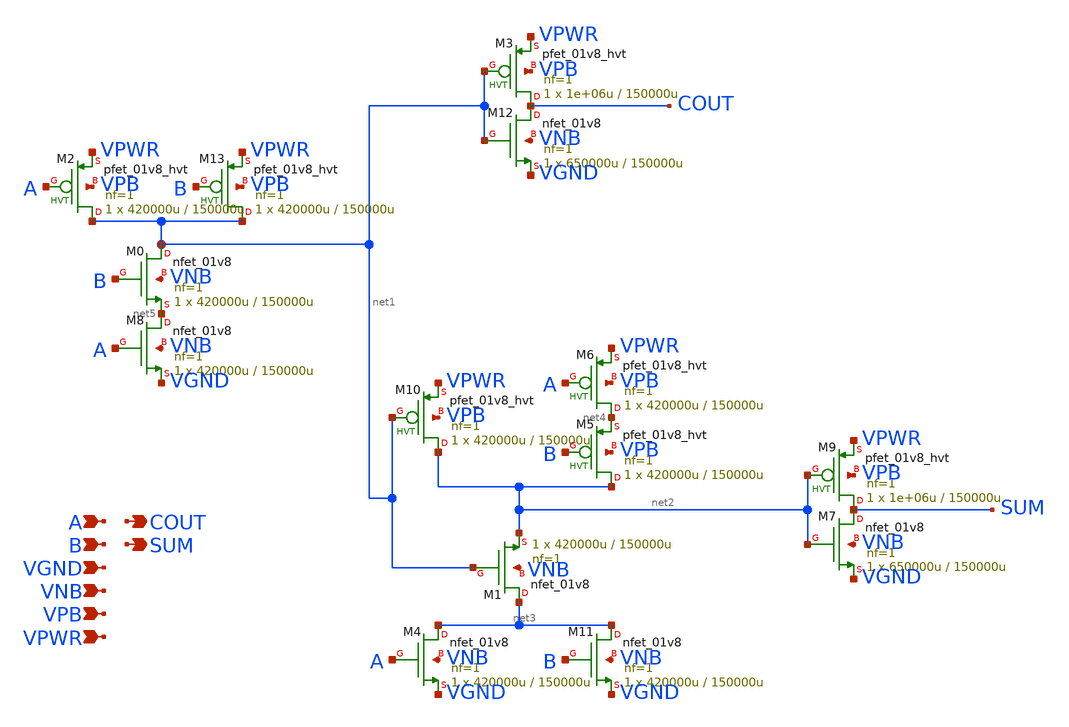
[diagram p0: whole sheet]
** sch_path: schematics/ha/sky130_fd_sc_hd__ha_1.sch
**.subckt sky130_fd_sc_hd__ha_1 A B VGND VNB VPB VPWR COUT SUM
*.ipin A
*.ipin B
*.ipin VGND
*.ipin VNB
*.ipin VPB
*.ipin VPWR
*.opin COUT
*.opin SUM
XM3 COUT net1 VPWR VPB sky130_fd_pr__pfet_01v8_hvt L=150000u W=1e+06u nf=1 ad='int((1 + 1)/2) * 1e+06u / 1 * 0.29'
+ as='int((1 + 2)/2) * 1e+06u / 1 * 0.29' pd='2*int((1 + 1)/2) * (1e+06u / 1 + 0.29)' ps='2*int((1 + 2)/2) * (1e+06u / 1 + 0.29)'
+ nrd='0.29 / 1e+06u ' nrs='0.29 / 1e+06u ' sa=0 sb=0 sd=0 mult=1 m=1
XM12 COUT net1 VGND VNB sky130_fd_pr__nfet_01v8 L=150000u W=650000u nf=1 ad='int((1 + 1)/2) * 650000u / 1 * 0.29'
+ as='int((1 + 2)/2) * 650000u / 1 * 0.29' pd='2*int((1 + 1)/2) * (650000u / 1 + 0.29)' ps='2*int((1 + 2)/2) * (650000u / 1 + 0.29)'
+ nrd='0.29 / 650000u ' nrs='0.29 / 650000u ' sa=0 sb=0 sd=0 mult=1 m=1
XM9 SUM net2 VPWR VPB sky130_fd_pr__pfet_01v8_hvt L=150000u W=1e+06u nf=1 ad='int((1 + 1)/2) * 1e+06u / 1 * 0.29'
+ as='int((1 + 2)/2) * 1e+06u / 1 * 0.29' pd='2*int((1 + 1)/2) * (1e+06u / 1 + 0.29)' ps='2*int((1 + 2)/2) * (1e+06u / 1 + 0.29)'
+ nrd='0.29 / 1e+06u ' nrs='0.29 / 1e+06u ' sa=0 sb=0 sd=0 mult=1 m=1
XM7 SUM net2 VGND VNB sky130_fd_pr__nfet_01v8 L=150000u W=650000u nf=1 ad='int((1 + 1)/2) * 650000u / 1 * 0.29'
+ as='int((1 + 2)/2) * 650000u / 1 * 0.29' pd='2*int((1 + 1)/2) * (650000u / 1 + 0.29)' ps='2*int((1 + 2)/2) * (650000u / 1 + 0.29)'
+ nrd='0.29 / 650000u ' nrs='0.29 / 650000u ' sa=0 sb=0 sd=0 mult=1 m=1
XM2 net1 A VPWR VPB sky130_fd_pr__pfet_01v8_hvt L=150000u W=420000u nf=1 ad='int((1 + 1)/2) * 420000u / 1 * 0.29'
+ as='int((1 + 2)/2) * 420000u / 1 * 0.29' pd='2*int((1 + 1)/2) * (420000u / 1 + 0.29)' ps='2*int((1 + 2)/2) * (420000u / 1 + 0.29)'
+ nrd='0.29 / 420000u ' nrs='0.29 / 420000u ' sa=0 sb=0 sd=0 mult=1 m=1
XM6 net4 A VPWR VPB sky130_fd_pr__pfet_01v8_hvt L=150000u W=420000u nf=1 ad='int((1 + 1)/2) * 420000u / 1 * 0.29'
+ as='int((1 + 2)/2) * 420000u / 1 * 0.29' pd='2*int((1 + 1)/2) * (420000u / 1 + 0.29)' ps='2*int((1 + 2)/2) * (420000u / 1 + 0.29)'
+ nrd='0.29 / 420000u ' nrs='0.29 / 420000u ' sa=0 sb=0 sd=0 mult=1 m=1
XM10 net2 net1 VPWR VPB sky130_fd_pr__pfet_01v8_hvt L=150000u W=420000u nf=1 ad='int((1 + 1)/2) * 420000u / 1 * 0.29'
+ as='int((1 + 2)/2) * 420000u / 1 * 0.29' pd='2*int((1 + 1)/2) * (420000u / 1 + 0.29)' ps='2*int((1 + 2)/2) * (420000u / 1 + 0.29)'
+ nrd='0.29 / 420000u ' nrs='0.29 / 420000u ' sa=0 sb=0 sd=0 mult=1 m=1
XM5 net2 B net4 VPB sky130_fd_pr__pfet_01v8_hvt L=150000u W=420000u nf=1 ad='int((1 + 1)/2) * 420000u / 1 * 0.29'
+ as='int((1 + 2)/2) * 420000u / 1 * 0.29' pd='2*int((1 + 1)/2) * (420000u / 1 + 0.29)' ps='2*int((1 + 2)/2) * (420000u / 1 + 0.29)'
+ nrd='0.29 / 420000u ' nrs='0.29 / 420000u ' sa=0 sb=0 sd=0 mult=1 m=1
XM13 net1 B VPWR VPB sky130_fd_pr__pfet_01v8_hvt L=150000u W=420000u nf=1 ad='int((1 + 1)/2) * 420000u / 1 * 0.29'
+ as='int((1 + 2)/2) * 420000u / 1 * 0.29' pd='2*int((1 + 1)/2) * (420000u / 1 + 0.29)' ps='2*int((1 + 2)/2) * (420000u / 1 + 0.29)'
+ nrd='0.29 / 420000u ' nrs='0.29 / 420000u ' sa=0 sb=0 sd=0 mult=1 m=1
XM4 net3 A VGND VNB sky130_fd_pr__nfet_01v8 L=150000u W=420000u nf=1 ad='int((1 + 1)/2) * 420000u / 1 * 0.29'
+ as='int((1 + 2)/2) * 420000u / 1 * 0.29' pd='2*int((1 + 1)/2) * (420000u / 1 + 0.29)' ps='2*int((1 + 2)/2) * (420000u / 1 + 0.29)'
+ nrd='0.29 / 420000u ' nrs='0.29 / 420000u ' sa=0 sb=0 sd=0 mult=1 m=1
XM8 net5 A VGND VNB sky130_fd_pr__nfet_01v8 L=150000u W=420000u nf=1 ad='int((1 + 1)/2) * 420000u / 1 * 0.29'
+ as='int((1 + 2)/2) * 420000u / 1 * 0.29' pd='2*int((1 + 1)/2) * (420000u / 1 + 0.29)' ps='2*int((1 + 2)/2) * (420000u / 1 + 0.29)'
+ nrd='0.29 / 420000u ' nrs='0.29 / 420000u ' sa=0 sb=0 sd=0 mult=1 m=1
XM1 net3 net1 net2 VNB sky130_fd_pr__nfet_01v8 L=150000u W=420000u nf=1 ad='int((1 + 1)/2) * 420000u / 1 * 0.29'
+ as='int((1 + 2)/2) * 420000u / 1 * 0.29' pd='2*int((1 + 1)/2) * (420000u / 1 + 0.29)' ps='2*int((1 + 2)/2) * (420000u / 1 + 0.29)'
+ nrd='0.29 / 420000u ' nrs='0.29 / 420000u ' sa=0 sb=0 sd=0 mult=1 m=1
XM0 net1 B net5 VNB sky130_fd_pr__nfet_01v8 L=150000u W=420000u nf=1 ad='int((1 + 1)/2) * 420000u / 1 * 0.29'
+ as='int((1 + 2)/2) * 420000u / 1 * 0.29' pd='2*int((1 + 1)/2) * (420000u / 1 + 0.29)' ps='2*int((1 + 2)/2) * (420000u / 1 + 0.29)'
+ nrd='0.29 / 420000u ' nrs='0.29 / 420000u ' sa=0 sb=0 sd=0 mult=1 m=1
XM11 net3 B VGND VNB sky130_fd_pr__nfet_01v8 L=150000u W=420000u nf=1 ad='int((1 + 1)/2) * 420000u / 1 * 0.29'
+ as='int((1 + 2)/2) * 420000u / 1 * 0.29' pd='2*int((1 + 1)/2) * (420000u / 1 + 0.29)' ps='2*int((1 + 2)/2) * (420000u / 1 + 0.29)'
+ nrd='0.29 / 420000u ' nrs='0.29 / 420000u ' sa=0 sb=0 sd=0 mult=1 m=1
**.ends
.end
